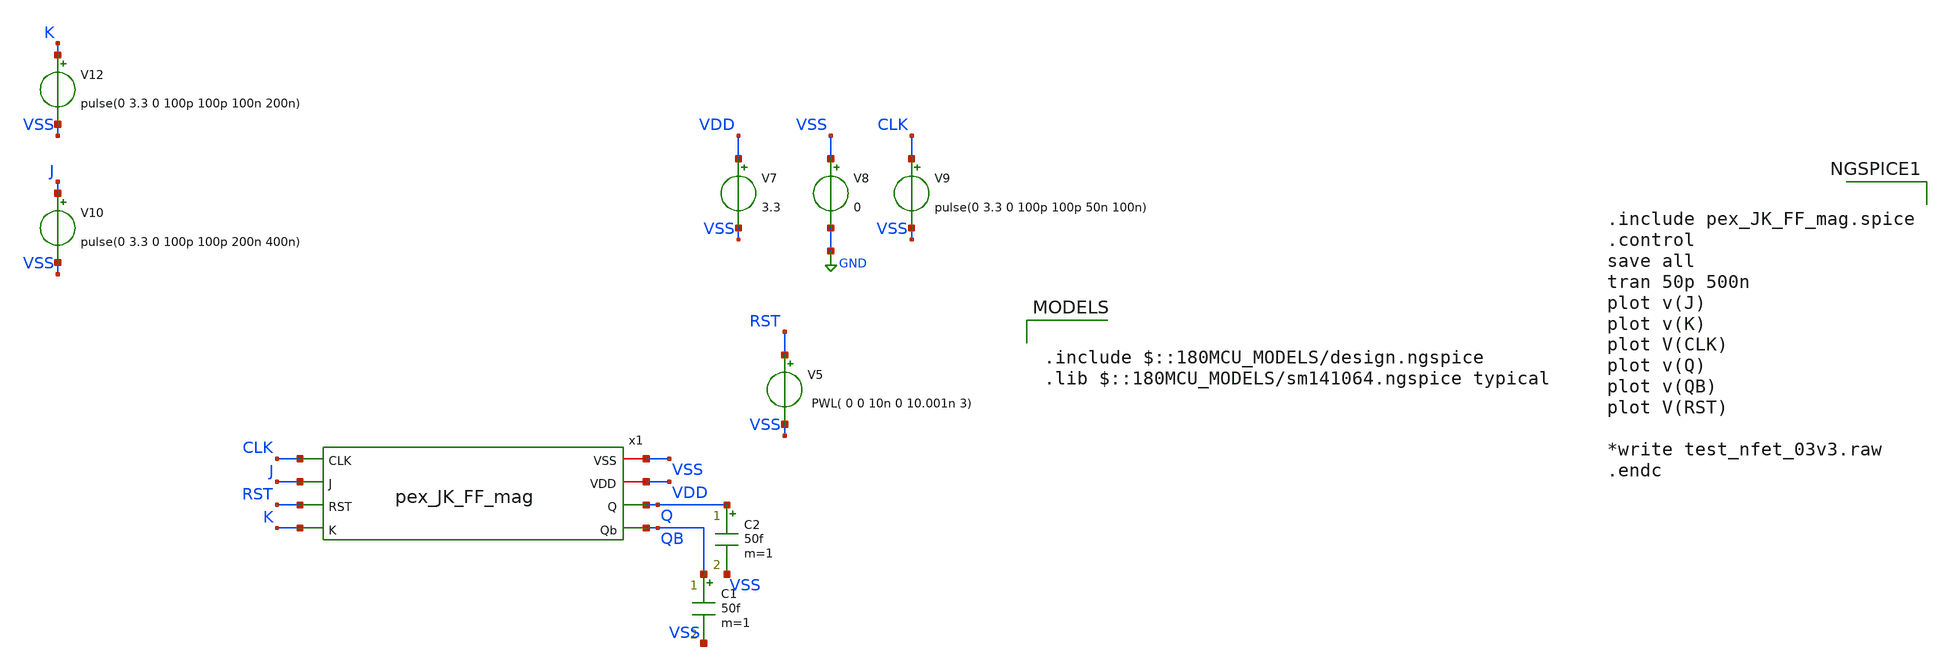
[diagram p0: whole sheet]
** sch_path: Clock_Generator_PAKISTAN_02/Schematics/JK_FF_PEX_TB.sch
**.subckt JK_FF_PEX_TB
C1 QB VSS 50f m=1
C2 Q VSS 50f m=1
x1 CLK VSS VDD Q J QB RST K pex_JK_FF_mag
V7 VDD VSS 3.3
V8 VSS GND 0
V9 CLK VSS pulse(0 3.3 0 100p 100p 50n 100n)
V10 J VSS pulse(0 3.3 0 100p 100p 200n 400n)
V12 K VSS pulse(0 3.3 0 100p 100p 100n 200n)
V5 RST VSS PWL( 0 0 10n 0 10.001n 3)
**** begin user architecture code

.include $::180MCU_MODELS/design.ngspice
.lib $::180MCU_MODELS/sm141064.ngspice typical



.include pex_JK_FF_mag.spice
.control
save all
tran 50p 500n
plot v(J)
plot v(K)
plot V(CLK)
plot v(Q)
plot v(QB)
plot V(RST)

*write test_nfet_03v3.raw
.endc


**** end user architecture code
**.ends
.GLOBAL GND
.end
